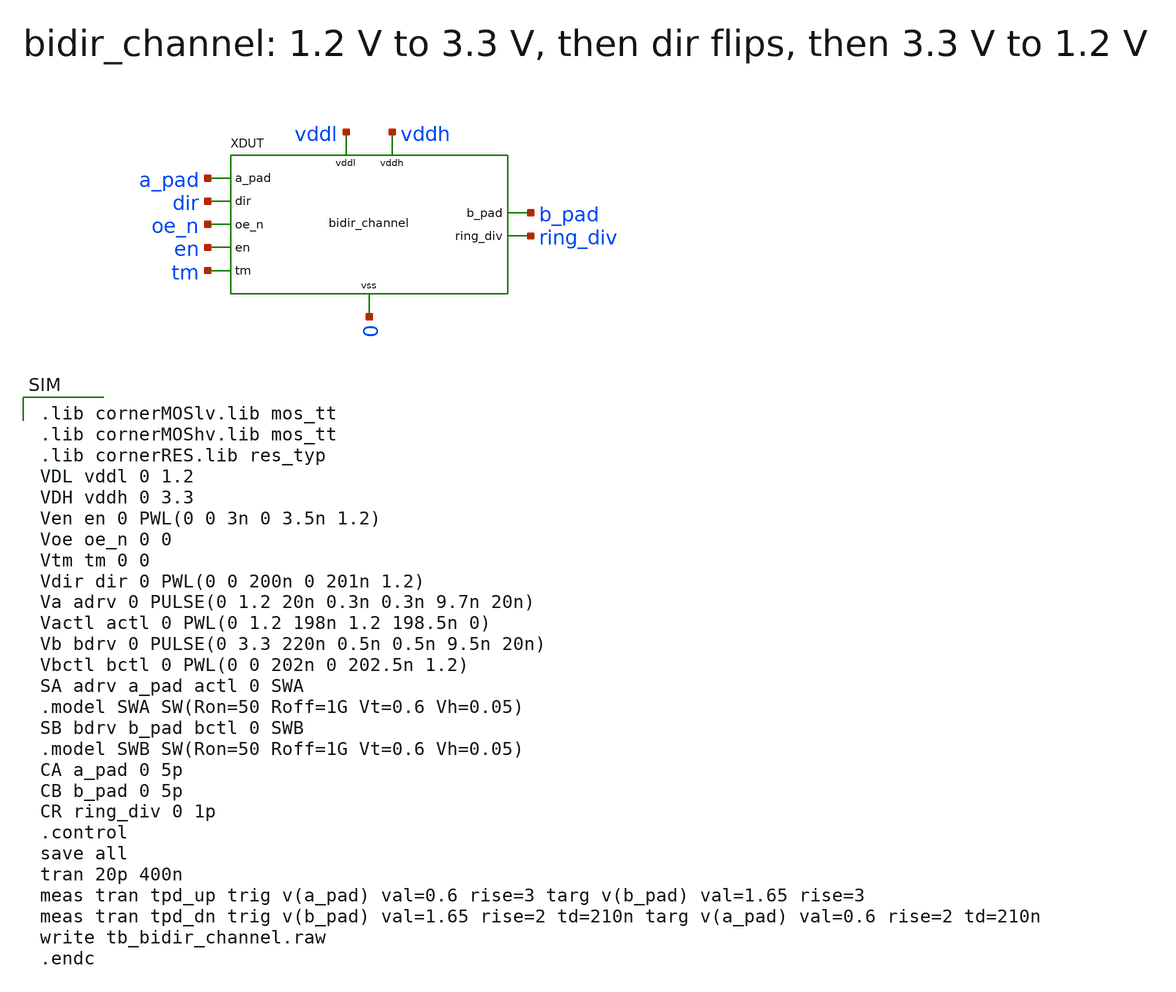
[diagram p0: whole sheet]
** sch_path: verification/tb_bidir_channel.sch
**.subckt tb_bidir_channel
XDUT a_pad b_pad dir oe_n en tm ring_div vddl vddh 0 bidir_channel
**** begin user architecture code

.lib cornerMOSlv.lib mos_tt
.lib cornerMOShv.lib mos_tt
.lib cornerRES.lib res_typ
VDL vddl 0 1.2
VDH vddh 0 3.3
Ven en 0 PWL(0 0 3n 0 3.5n 1.2)
Voe oe_n 0 0
Vtm tm 0 0
Vdir dir 0 PWL(0 0 200n 0 201n 1.2)
Va adrv 0 PULSE(0 1.2 20n 0.3n 0.3n 9.7n 20n)
Vactl actl 0 PWL(0 1.2 198n 1.2 198.5n 0)
Vb bdrv 0 PULSE(0 3.3 220n 0.5n 0.5n 9.5n 20n)
Vbctl bctl 0 PWL(0 0 202n 0 202.5n 1.2)
SA adrv a_pad actl 0 SWA
.model SWA SW(Ron=50 Roff=1G Vt=0.6 Vh=0.05)
SB bdrv b_pad bctl 0 SWB
.model SWB SW(Ron=50 Roff=1G Vt=0.6 Vh=0.05)
CA a_pad 0 5p
CB b_pad 0 5p
CR ring_div 0 1p
.control
save all
tran 20p 400n
meas tran tpd_up trig v(a_pad) val=0.6 rise=3 targ v(b_pad) val=1.65 rise=3
meas tran tpd_dn trig v(b_pad) val=1.65 rise=2 td=210n targ v(a_pad) val=0.6 rise=2 td=210n
write tb_bidir_channel.raw
.endc

**** end user architecture code
**.ends
.end
